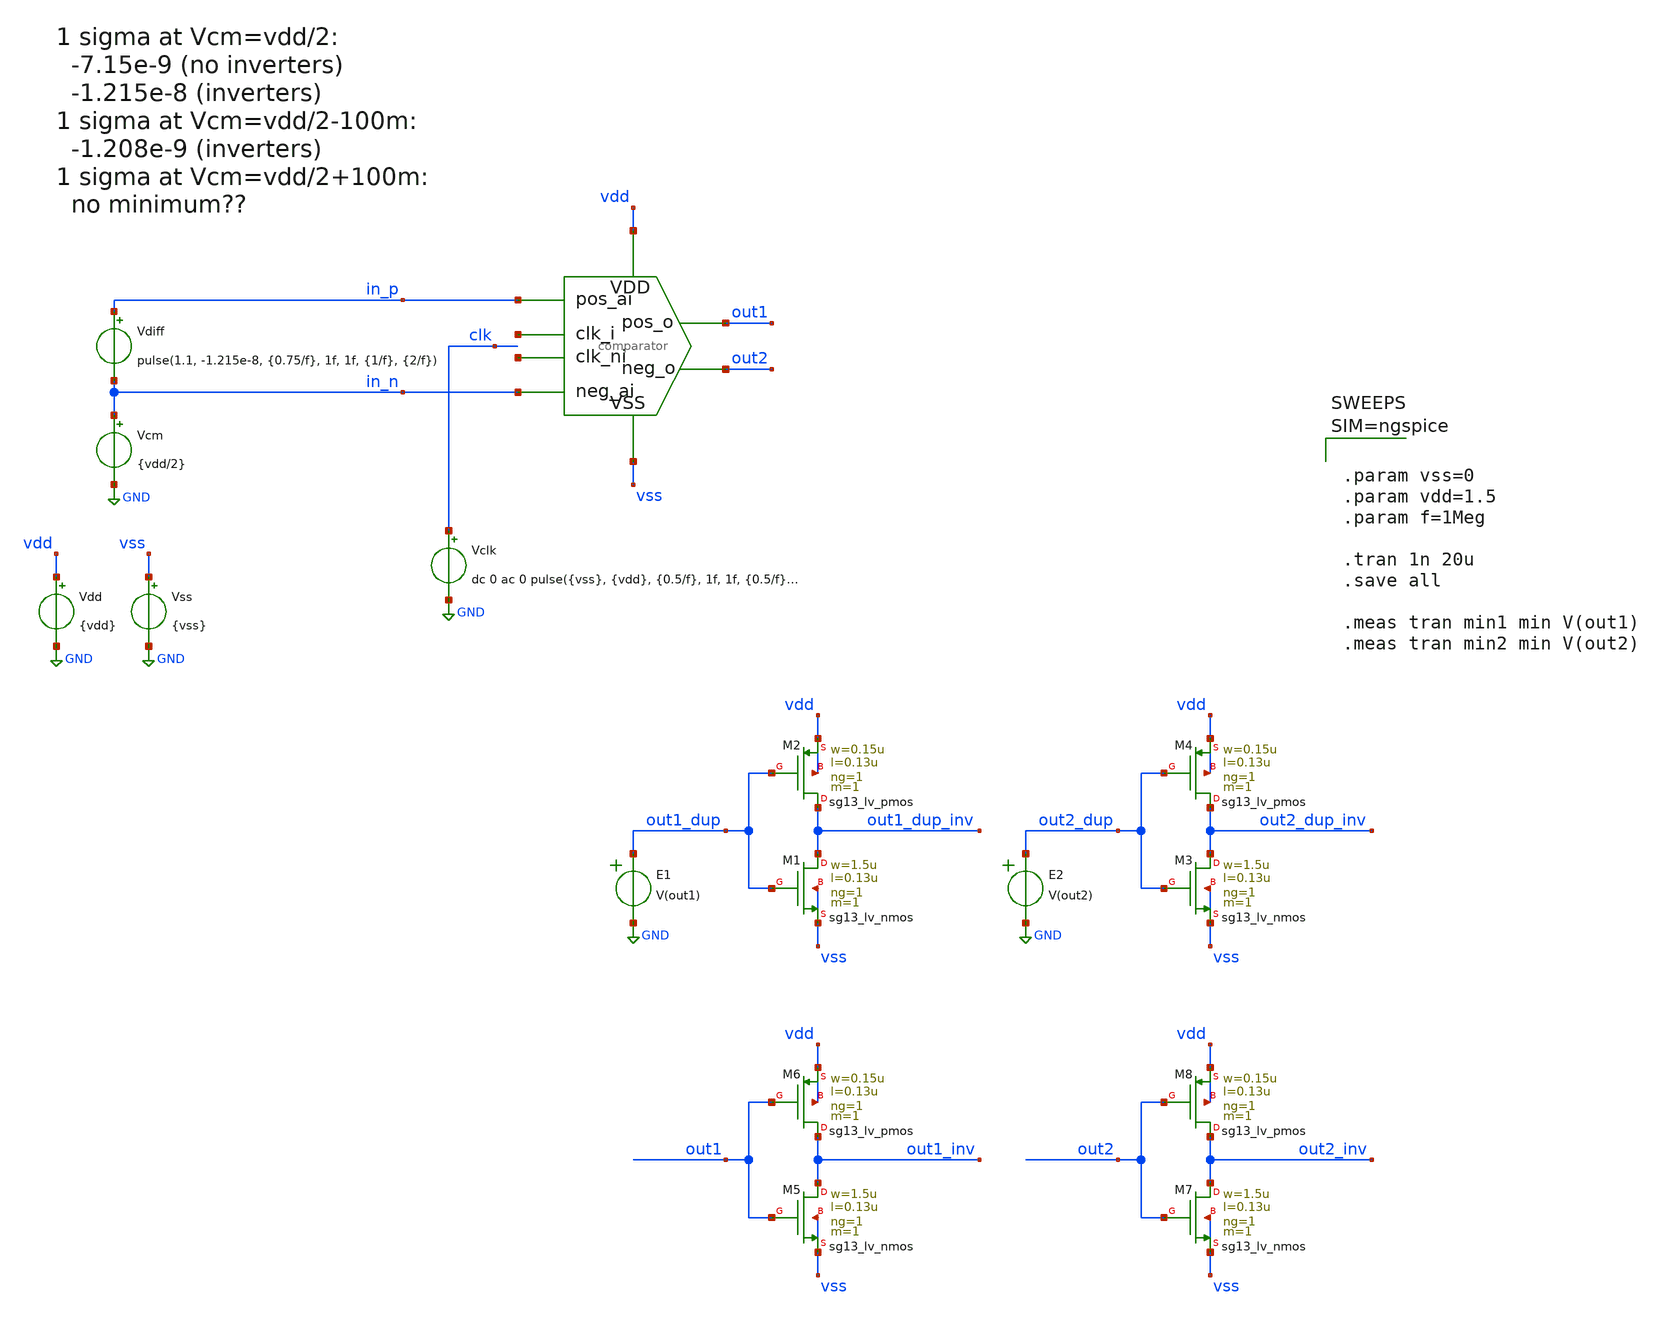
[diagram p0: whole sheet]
** sch_path: designs/comparator/comparator_tb.sch
**.subckt comparator_tb
x1 net1 in_p in_n out2 out1 vss vdd net2 comparator
Vdd vdd GND {vdd}
Vss vss GND {vss}
Vclk clk GND dc 0 ac 0 pulse({vss}, {vdd}, {0.5/f}, 1f, 1f, {0.5/f}, {1/f})
Vdiff in_p in_n pulse(1.1, -1.215e-8, {0.75/f}, 1f, 1f, {1/f}, {2/f})
Vcm in_n GND {vdd/2}
E1 out1_dup GND VOL=' V(out1) '
XM1 out1_dup_inv out1_dup vss vss sg13_lv_nmos w=1.5u l=0.13u ng=1 m=1 mm_ok=1
XM2 out1_dup_inv out1_dup vdd vdd sg13_lv_pmos w=0.15u l=0.13u ng=1 m=1 mm_ok=1
E2 out2_dup GND VOL=' V(out2) '
XM3 out2_dup_inv out2_dup vss vss sg13_lv_nmos w=1.5u l=0.13u ng=1 m=1 mm_ok=1
XM4 out2_dup_inv out2_dup vdd vdd sg13_lv_pmos w=0.15u l=0.13u ng=1 m=1 mm_ok=1
XM5 out1_inv out1 vss vss sg13_lv_nmos w=1.5u l=0.13u ng=1 m=1 mm_ok=1
XM6 out1_inv out1 vdd vdd sg13_lv_pmos w=0.15u l=0.13u ng=1 m=1 mm_ok=1
XM7 out2_inv out2 vss vss sg13_lv_nmos w=1.5u l=0.13u ng=1 m=1 mm_ok=1
XM8 out2_inv out2 vdd vdd sg13_lv_pmos w=0.15u l=0.13u ng=1 m=1 mm_ok=1
**** begin user architecture code

.lib $::SG13G2_MODELS/cornerMOSlv.lib mos_tt
.include $::PDK_ROOT/ihp-sg13g2/libs.ref/sg13g2_stdcell/spice/sg13g2_stdcell.spice




.param vss=0
.param vdd=1.5
.param f=1Meg

.tran 1n 20u
.save all

.meas tran min1 min V(out1)
.meas tran min2 min V(out2)



**** end user architecture code
**.ends

* expanding   symbol:  comparator.sym # of pins=8
** sym_path: designs/comparator_dt/comparator.sym
** sch_path: designs/comparator_dt/comparator.sch
.subckt comparator clk_i pos_ai neg_ai neg_o pos_o VSS VDD clk_ni
*.ipin pos_ai
*.ipin neg_ai
*.ipin VSS
*.ipin VDD
*.opin neg_o
*.opin pos_o
*.ipin clk_i
*.ipin clk_ni
XM12 neg_buf clk_i VDD VDD sg13_lv_pmos w=1.0u l=0.13u ng=1 m=1 mm_ok=1
XM13 pos_buf clk_i VDD VDD sg13_lv_pmos w=1.0u l=0.13u ng=1 m=1 mm_ok=1
XM14 net1 pos_ai neg_buf VSS sg13_lv_nmos w=1.0u l=0.13u ng=1 m=1 mm_ok=1
XM15 net1 neg_ai pos_buf VSS sg13_lv_nmos w=1.0u l=0.13u ng=1 m=1 mm_ok=1
XM16 VSS clk_i net1 VSS sg13_lv_nmos w=1.0u l=0.13u ng=1 m=1 mm_ok=1
XM17 net2 clk_ni VDD VDD sg13_lv_pmos w=2.0u l=0.13u ng=2 m=1 mm_ok=1
XM18 pos_o neg_o net2 VDD sg13_lv_pmos w=2.0u l=0.13u ng=2 m=1 mm_ok=1
XM19 neg_o pos_o net2 VDD sg13_lv_pmos w=2.0u l=0.13u ng=2 m=1 mm_ok=1
XM20 VSS neg_buf pos_o VSS sg13_lv_nmos w=1.0u l=0.13u ng=1 m=1 mm_ok=1
XM21 VSS neg_o pos_o VSS sg13_lv_nmos w=1.0u l=0.13u ng=1 m=1 mm_ok=1
XM22 VSS pos_o neg_o VSS sg13_lv_nmos w=1.0u l=0.13u ng=1 m=1 mm_ok=1
XM23 VSS pos_buf neg_o VSS sg13_lv_nmos w=1.0u l=0.13u ng=1 m=1 mm_ok=1
XC1 neg_buf VSS cap_cmim w=1.41e-5 l=1.41e-5 m=1 mm_ok=1
XC2 pos_buf VSS cap_cmim w=1.41e-5 l=1.41e-5 m=1 mm_ok=1
.ends

.GLOBAL GND
.end
